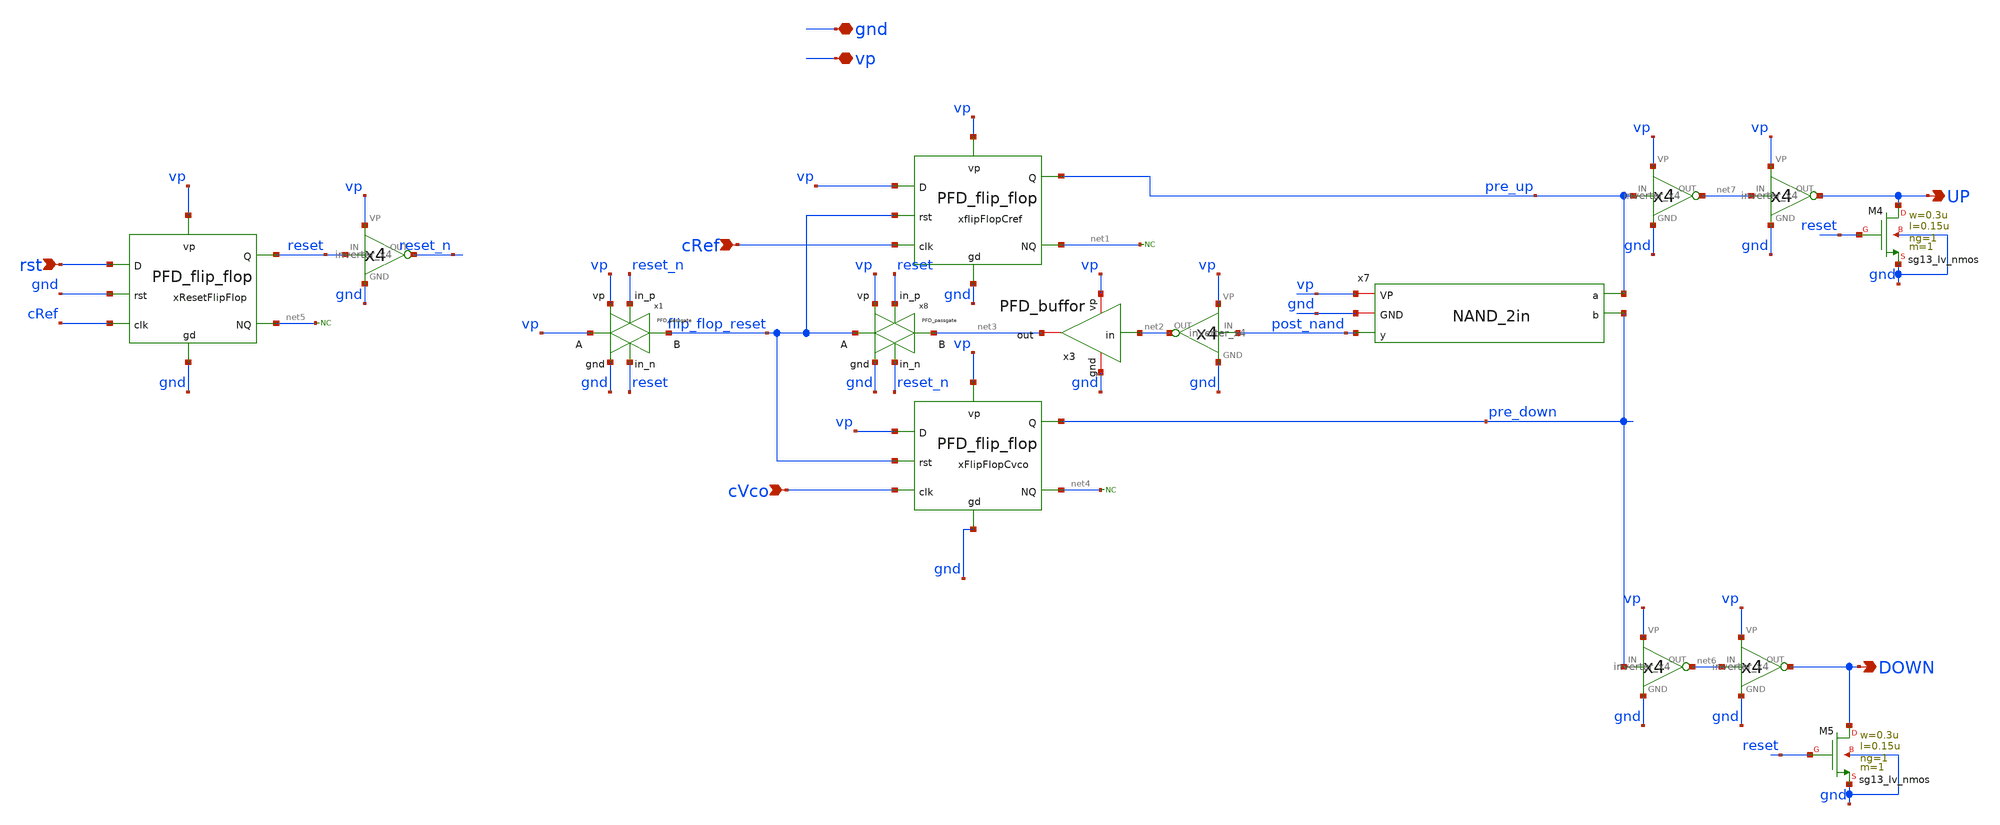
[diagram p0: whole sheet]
** sch_path: schematics/PFD/PFD_cell_2.sch
**.subckt PFD_cell_2 gnd vp cRef cVco rst UP DOWN
*.iopin gnd
*.iopin vp
*.ipin cRef
*.ipin cVco
*.ipin rst
*.opin UP
*.opin DOWN
x7 vp gnd pre_up post_nand pre_down NAND_2in
* noconn #net1
* noconn #net4
x9 reset reset_n vp gnd inverter_x4
xflipFlopCref cRef flip_flop_reset vp pre_up net1 vp gnd PFD_flip_flop
xFlipFlopCvco cVco flip_flop_reset vp pre_down net4 vp gnd PFD_flip_flop
x1 reset vp vp flip_flop_reset gnd reset_n PFD_passgate
x11 post_nand net2 vp gnd inverter_x4
XM4 UP reset gnd gnd sg13_lv_nmos w=0.3u l=0.15u ng=1 m=1 mm_ok=1
XM5 DOWN reset gnd gnd sg13_lv_nmos w=0.3u l=0.15u ng=1 m=1 mm_ok=1
x8 reset_n vp flip_flop_reset net3 gnd reset PFD_passgate
* noconn #net5
xResetFlipFlop cRef gnd rst reset net5 vp gnd PFD_flip_flop
x3 gnd vp net3 net2 PFD_buffor
x4 net7 UP vp gnd inverter_x4
x6 net6 DOWN vp gnd inverter_x4
x2 pre_up net7 vp gnd inverter_x4
x5 pre_down net6 vp gnd inverter_x4
**.ends
.end
